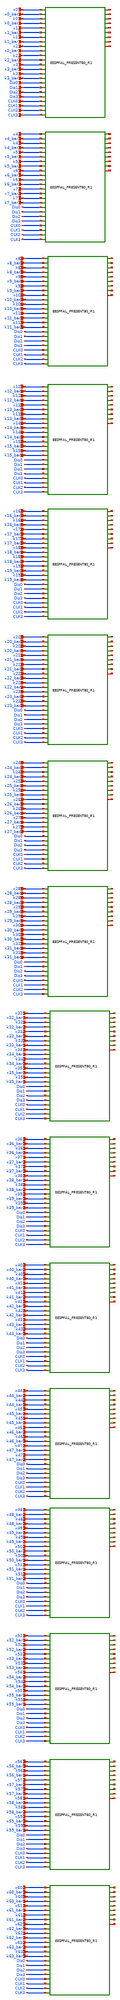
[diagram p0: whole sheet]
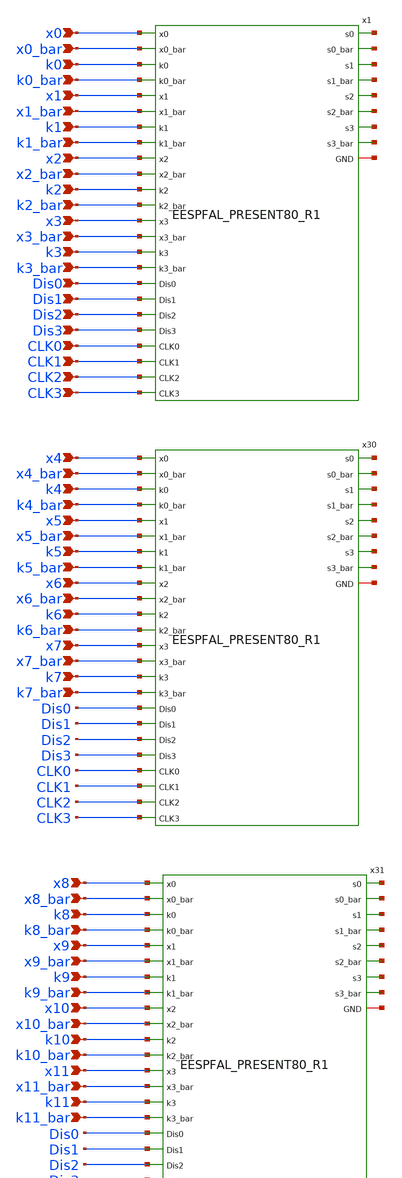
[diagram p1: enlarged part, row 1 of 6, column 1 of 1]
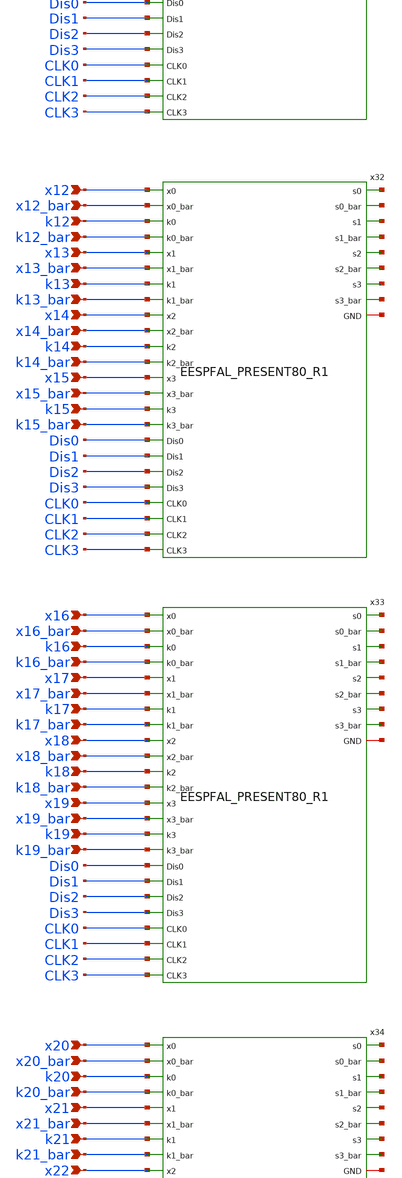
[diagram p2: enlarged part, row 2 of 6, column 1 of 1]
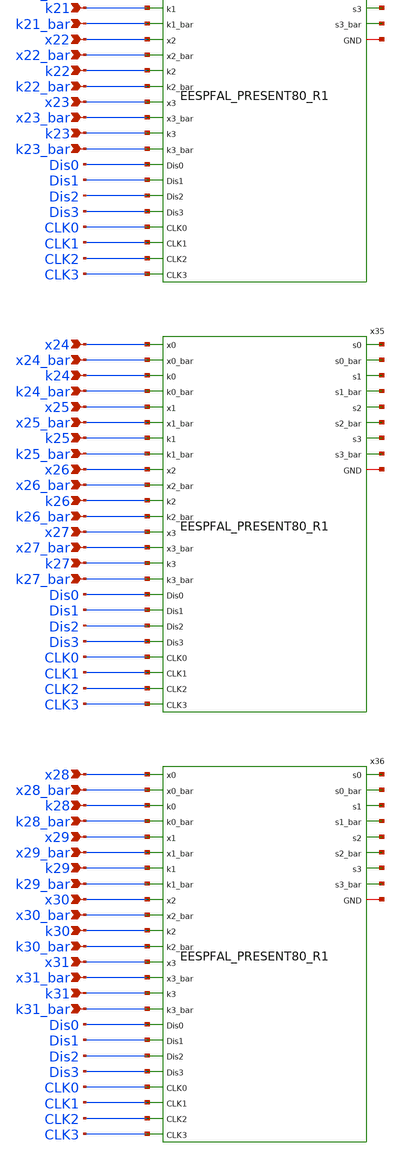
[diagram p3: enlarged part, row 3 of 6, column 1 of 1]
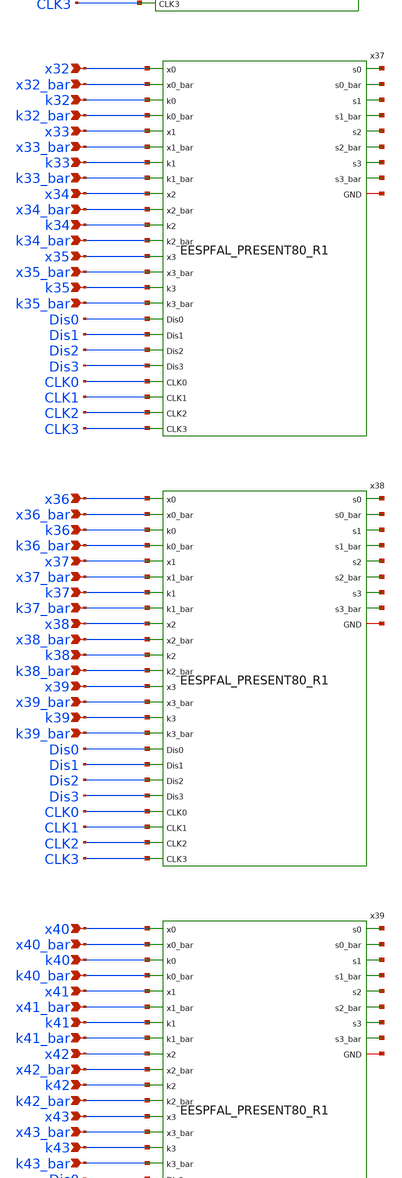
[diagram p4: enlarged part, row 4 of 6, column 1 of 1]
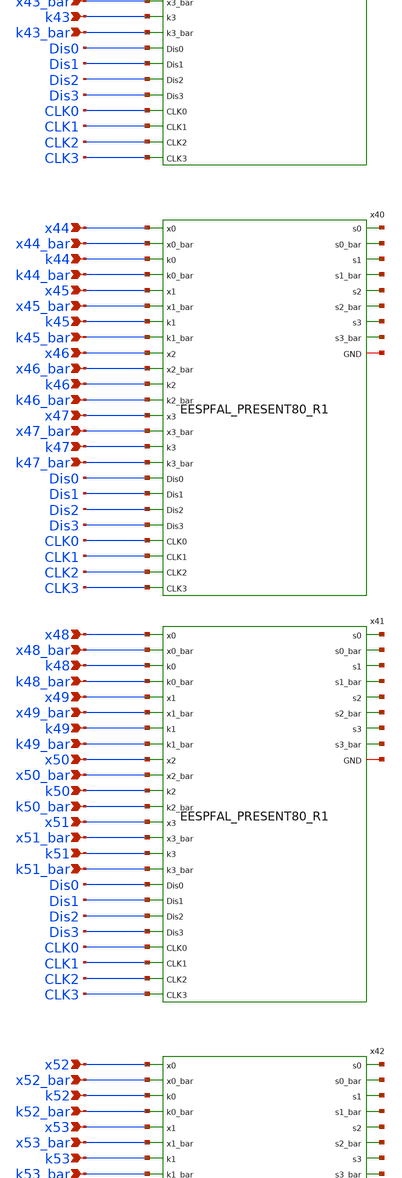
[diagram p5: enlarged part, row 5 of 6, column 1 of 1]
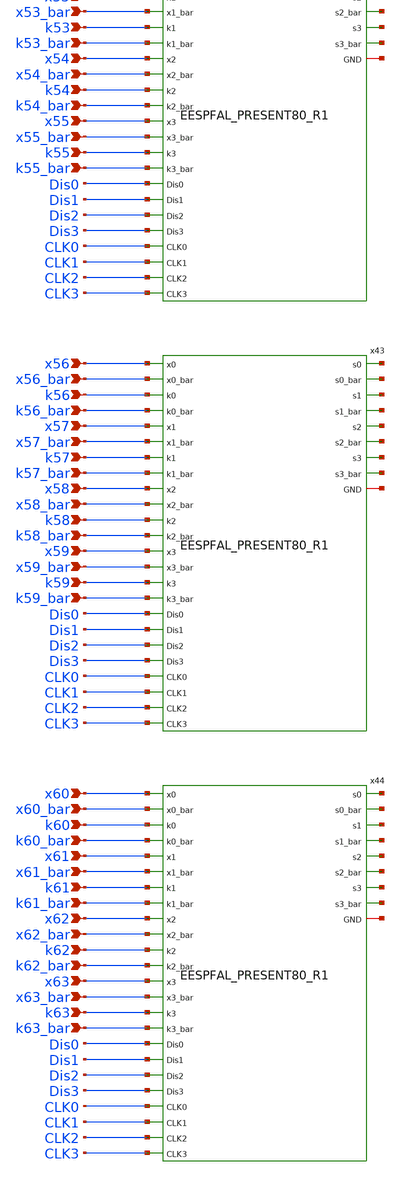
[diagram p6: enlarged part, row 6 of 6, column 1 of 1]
** sch_path: skywater_stuff/untitled-24.sch
**.subckt untitled-24 x4 x4_bar k4 k4_bar x5 x5_bar k5 k5_bar x6 x6_bar k6 k6_bar x7 x7_bar k7
*+ k7_bar x8 x8_bar k8 k8_bar x9 x9_bar k9 k9_bar x10 x10_bar k10 k10_bar x11 x11_bar k11 k11_bar x12 x12_bar
*+ k12 k12_bar x13 x13_bar k13 k13_bar x14 x14_bar k14 k14_bar x15 x15_bar k15 k15_bar x16 x16_bar k16
*+ k16_bar x17 x17_bar k17 k17_bar x18 x18_bar k18 k18_bar x19 x19_bar k19 k19_bar x20 x20_bar k20 k20_bar x21
*+ x21_bar k21 k21_bar x22 x22_bar k22 k22_bar x23 x23_bar k23 k23_bar x24 x24_bar k24 k24_bar x25 x25_bar k25
*+ k25_bar x26 x26_bar k26 k26_bar x27 x27_bar k27 k27_bar x28 x28_bar k28 k28_bar x29 x29_bar k29 k29_bar x30
*+ x30_bar k30 k30_bar x31 x31_bar k31 k31_bar x32 x32_bar k32 k32_bar x33 x33_bar k33 k33_bar x34 x34_bar k34
*+ k34_bar x35 x35_bar k35 k35_bar x36 x36_bar k36 k36_bar x37 x37_bar k37 k37_bar x38 x38_bar k38 k38_bar x39
*+ x39_bar k39 k39_bar x40 x40_bar k40 k40_bar x41 x41_bar k41 k41_bar x42 x42_bar k42 k42_bar x43 x43_bar k43
*+ k43_bar x44 x44_bar k44 k44_bar x45 x45_bar k45 k45_bar x46 x46_bar k46 k46_bar x47 x47_bar k47 k47_bar x48
*+ x48_bar k48 k48_bar x49 x49_bar k49 k49_bar x50 x50_bar k50 k50_bar x51 x51_bar k51 k51_bar x52 x52_bar k52
*+ k52_bar x53 x53_bar k53 k53_bar x54 x54_bar k54 k54_bar x55 x55_bar k55 k55_bar x56 x56_bar k56 k56_bar x57
*+ x57_bar k57 k57_bar x58 x58_bar k58 k58_bar x59 x59_bar k59 k59_bar x60 x60_bar k60 k60_bar x61 x61_bar k61
*+ k61_bar x62 x62_bar k62 k62_bar x63 x63_bar k63 k63_bar x0 x0_bar k0 k0_bar x1 x1_bar k1 k1_bar x2 x2_bar
*+ k2 k2_bar x3 x3_bar k3 k3_bar Dis0 Dis1 CLK0 Dis2 Dis3 CLK1 CLK2 CLK3
*.ipin x4
*.ipin x4_bar
*.ipin k4
*.ipin k4_bar
*.ipin x5
*.ipin x5_bar
*.ipin k5
*.ipin k5_bar
*.ipin x6
*.ipin x6_bar
*.ipin k6
*.ipin k6_bar
*.ipin x7
*.ipin x7_bar
*.ipin k7
*.ipin k7_bar
*.ipin x8
*.ipin x8_bar
*.ipin k8
*.ipin k8_bar
*.ipin x9
*.ipin x9_bar
*.ipin k9
*.ipin k9_bar
*.ipin x10
*.ipin x10_bar
*.ipin k10
*.ipin k10_bar
*.ipin x11
*.ipin x11_bar
*.ipin k11
*.ipin k11_bar
*.ipin x12
*.ipin x12_bar
*.ipin k12
*.ipin k12_bar
*.ipin x13
*.ipin x13_bar
*.ipin k13
*.ipin k13_bar
*.ipin x14
*.ipin x14_bar
*.ipin k14
*.ipin k14_bar
*.ipin x15
*.ipin x15_bar
*.ipin k15
*.ipin k15_bar
*.ipin x16
*.ipin x16_bar
*.ipin k16
*.ipin k16_bar
*.ipin x17
*.ipin x17_bar
*.ipin k17
*.ipin k17_bar
*.ipin x18
*.ipin x18_bar
*.ipin k18
*.ipin k18_bar
*.ipin x19
*.ipin x19_bar
*.ipin k19
*.ipin k19_bar
*.ipin x20
*.ipin x20_bar
*.ipin k20
*.ipin k20_bar
*.ipin x21
*.ipin x21_bar
*.ipin k21
*.ipin k21_bar
*.ipin x22
*.ipin x22_bar
*.ipin k22
*.ipin k22_bar
*.ipin x23
*.ipin x23_bar
*.ipin k23
*.ipin k23_bar
*.ipin x24
*.ipin x24_bar
*.ipin k24
*.ipin k24_bar
*.ipin x25
*.ipin x25_bar
*.ipin k25
*.ipin k25_bar
*.ipin x26
*.ipin x26_bar
*.ipin k26
*.ipin k26_bar
*.ipin x27
*.ipin x27_bar
*.ipin k27
*.ipin k27_bar
*.ipin x28
*.ipin x28_bar
*.ipin k28
*.ipin k28_bar
*.ipin x29
*.ipin x29_bar
*.ipin k29
*.ipin k29_bar
*.ipin x30
*.ipin x30_bar
*.ipin k30
*.ipin k30_bar
*.ipin x31
*.ipin x31_bar
*.ipin k31
*.ipin k31_bar
*.ipin x32
*.ipin x32_bar
*.ipin k32
*.ipin k32_bar
*.ipin x33
*.ipin x33_bar
*.ipin k33
*.ipin k33_bar
*.ipin x34
*.ipin x34_bar
*.ipin k34
*.ipin k34_bar
*.ipin x35
*.ipin x35_bar
*.ipin k35
*.ipin k35_bar
*.ipin x36
*.ipin x36_bar
*.ipin k36
*.ipin k36_bar
*.ipin x37
*.ipin x37_bar
*.ipin k37
*.ipin k37_bar
*.ipin x38
*.ipin x38_bar
*.ipin k38
*.ipin k38_bar
*.ipin x39
*.ipin x39_bar
*.ipin k39
*.ipin k39_bar
*.ipin x40
*.ipin x40_bar
*.ipin k40
*.ipin k40_bar
*.ipin x41
*.ipin x41_bar
*.ipin k41
*.ipin k41_bar
*.ipin x42
*.ipin x42_bar
*.ipin k42
*.ipin k42_bar
*.ipin x43
*.ipin x43_bar
*.ipin k43
*.ipin k43_bar
*.ipin x44
*.ipin x44_bar
*.ipin k44
*.ipin k44_bar
*.ipin x45
*.ipin x45_bar
*.ipin k45
*.ipin k45_bar
*.ipin x46
*.ipin x46_bar
*.ipin k46
*.ipin k46_bar
*.ipin x47
*.ipin x47_bar
*.ipin k47
*.ipin k47_bar
*.ipin x48
*.ipin x48_bar
*.ipin k48
*.ipin k48_bar
*.ipin x49
*.ipin x49_bar
*.ipin k49
*.ipin k49_bar
*.ipin x50
*.ipin x50_bar
*.ipin k50
*.ipin k50_bar
*.ipin x51
*.ipin x51_bar
*.ipin k51
*.ipin k51_bar
*.ipin x52
*.ipin x52_bar
*.ipin k52
*.ipin k52_bar
*.ipin x53
*.ipin x53_bar
*.ipin k53
*.ipin k53_bar
*.ipin x54
*.ipin x54_bar
*.ipin k54
*.ipin k54_bar
*.ipin x55
*.ipin x55_bar
*.ipin k55
*.ipin k55_bar
*.ipin x56
*.ipin x56_bar
*.ipin k56
*.ipin k56_bar
*.ipin x57
*.ipin x57_bar
*.ipin k57
*.ipin k57_bar
*.ipin x58
*.ipin x58_bar
*.ipin k58
*.ipin k58_bar
*.ipin x59
*.ipin x59_bar
*.ipin k59
*.ipin k59_bar
*.ipin x60
*.ipin x60_bar
*.ipin k60
*.ipin k60_bar
*.ipin x61
*.ipin x61_bar
*.ipin k61
*.ipin k61_bar
*.ipin x62
*.ipin x62_bar
*.ipin k62
*.ipin k62_bar
*.ipin x63
*.ipin x63_bar
*.ipin k63
*.ipin k63_bar
*.ipin x0
*.ipin x0_bar
*.ipin k0
*.ipin k0_bar
*.ipin x1
*.ipin x1_bar
*.ipin k1
*.ipin k1_bar
*.ipin x2
*.ipin x2_bar
*.ipin k2
*.ipin k2_bar
*.ipin x3
*.ipin x3_bar
*.ipin k3
*.ipin k3_bar
*.ipin Dis0
*.ipin Dis1
*.ipin CLK0
*.ipin Dis2
*.ipin Dis3
*.ipin CLK1
*.ipin CLK2
*.ipin CLK3
x1 net1 x0 x0_bar k0 k0_bar x1 x1_bar k1 k1_bar x2 x2_bar k2 k2_bar x3 x3_bar k3 k3_bar net2 net3
+ CLK0 Dis0 CLK1 Dis1 net4 net5 net6 net7 net8 net9 CLK3 Dis2 CLK2 Dis3 EESPFAL_PRESENT80_R1
x30 net10 x4 x4_bar k4 k4_bar x5 x5_bar k5 k5_bar x6 x6_bar k6 k6_bar x7 x7_bar k7 k7_bar net11
+ net12 CLK0 Dis0 CLK1 Dis1 net13 net14 net15 net16 net17 net18 CLK3 Dis2 CLK2 Dis3 EESPFAL_PRESENT80_R1
x31 net19 x8 x8_bar k8 k8_bar x9 x9_bar k9 k9_bar x10 x10_bar k10 k10_bar x11 x11_bar k11 k11_bar
+ net20 net21 CLK0 Dis0 CLK1 Dis1 net22 net23 net24 net25 net26 net27 CLK3 Dis2 CLK2 Dis3
+ EESPFAL_PRESENT80_R1
x32 net28 x12 x12_bar k12 k12_bar x13 x13_bar k13 k13_bar x14 x14_bar k14 k14_bar x15 x15_bar k15
+ k15_bar net29 net30 CLK0 Dis0 CLK1 Dis1 net31 net32 net33 net34 net35 net36 CLK3 Dis2 CLK2 Dis3
+ EESPFAL_PRESENT80_R1
x33 net37 x16 x16_bar k16 k16_bar x17 x17_bar k17 k17_bar x18 x18_bar k18 k18_bar x19 x19_bar k19
+ k19_bar net38 net39 CLK0 Dis0 CLK1 Dis1 net40 net41 net42 net43 net44 net45 CLK3 Dis2 CLK2 Dis3
+ EESPFAL_PRESENT80_R1
x34 net46 x20 x20_bar k20 k20_bar x21 x21_bar k21 k21_bar x22 x22_bar k22 k22_bar x23 x23_bar k23
+ k23_bar net47 net48 CLK0 Dis0 CLK1 Dis1 net49 net50 net51 net52 net53 net54 CLK3 Dis2 CLK2 Dis3
+ EESPFAL_PRESENT80_R1
x35 net55 x24 x24_bar k24 k24_bar x25 x25_bar k25 k25_bar x26 x26_bar k26 k26_bar x27 x27_bar k27
+ k27_bar net56 net57 CLK0 Dis0 CLK1 Dis1 net58 net59 net60 net61 net62 net63 CLK3 Dis2 CLK2 Dis3
+ EESPFAL_PRESENT80_R1
x36 net64 x28 x28_bar k28 k28_bar x29 x29_bar k29 k29_bar x30 x30_bar k30 k30_bar x31 x31_bar k31
+ k31_bar net65 net66 CLK0 Dis0 CLK1 Dis1 net67 net68 net69 net70 net71 net72 CLK3 Dis2 CLK2 Dis3
+ EESPFAL_PRESENT80_R1
x37 net73 x32 x32_bar k32 k32_bar x33 x33_bar k33 k33_bar x34 x34_bar k34 k34_bar x35 x35_bar k35
+ k35_bar net74 net75 CLK0 Dis0 CLK1 Dis1 net76 net77 net78 net79 net80 net81 CLK3 Dis2 CLK2 Dis3
+ EESPFAL_PRESENT80_R1
x38 net82 x36 x36_bar k36 k36_bar x37 x37_bar k37 k37_bar x38 x38_bar k38 k38_bar x39 x39_bar k39
+ k39_bar net83 net84 CLK0 Dis0 CLK1 Dis1 net85 net86 net87 net88 net89 net90 CLK3 Dis2 CLK2 Dis3
+ EESPFAL_PRESENT80_R1
x39 net91 x40 x40_bar k40 k40_bar x41 x41_bar k41 k41_bar x42 x42_bar k42 k42_bar x43 x43_bar k43
+ k43_bar net92 net93 CLK0 Dis0 CLK1 Dis1 net94 net95 net96 net97 net98 net99 CLK3 Dis2 CLK2 Dis3
+ EESPFAL_PRESENT80_R1
x40 net100 x44 x44_bar k44 k44_bar x45 x45_bar k45 k45_bar x46 x46_bar k46 k46_bar x47 x47_bar k47
+ k47_bar net101 net102 CLK0 Dis0 CLK1 Dis1 net103 net104 net105 net106 net107 net108 CLK3 Dis2 CLK2 Dis3
+ EESPFAL_PRESENT80_R1
x41 net109 x48 x48_bar k48 k48_bar x49 x49_bar k49 k49_bar x50 x50_bar k50 k50_bar x51 x51_bar k51
+ k51_bar net110 net111 CLK0 Dis0 CLK1 Dis1 net112 net113 net114 net115 net116 net117 CLK3 Dis2 CLK2 Dis3
+ EESPFAL_PRESENT80_R1
x42 net118 x52 x52_bar k52 k52_bar x53 x53_bar k53 k53_bar x54 x54_bar k54 k54_bar x55 x55_bar k55
+ k55_bar net119 net120 CLK0 Dis0 CLK1 Dis1 net121 net122 net123 net124 net125 net126 CLK3 Dis2 CLK2 Dis3
+ EESPFAL_PRESENT80_R1
x43 net127 x56 x56_bar k56 k56_bar x57 x57_bar k57 k57_bar x58 x58_bar k58 k58_bar x59 x59_bar k59
+ k59_bar net128 net129 CLK0 Dis0 CLK1 Dis1 net130 net131 net132 net133 net134 net135 CLK3 Dis2 CLK2 Dis3
+ EESPFAL_PRESENT80_R1
x44 net136 x60 x60_bar k60 k60_bar x61 x61_bar k61 k61_bar x62 x62_bar k62 k62_bar x63 x63_bar k63
+ k63_bar net137 net138 CLK0 Dis0 CLK1 Dis1 net139 net140 net141 net142 net143 net144 CLK3 Dis2 CLK2 Dis3
+ EESPFAL_PRESENT80_R1
**.ends
.end
